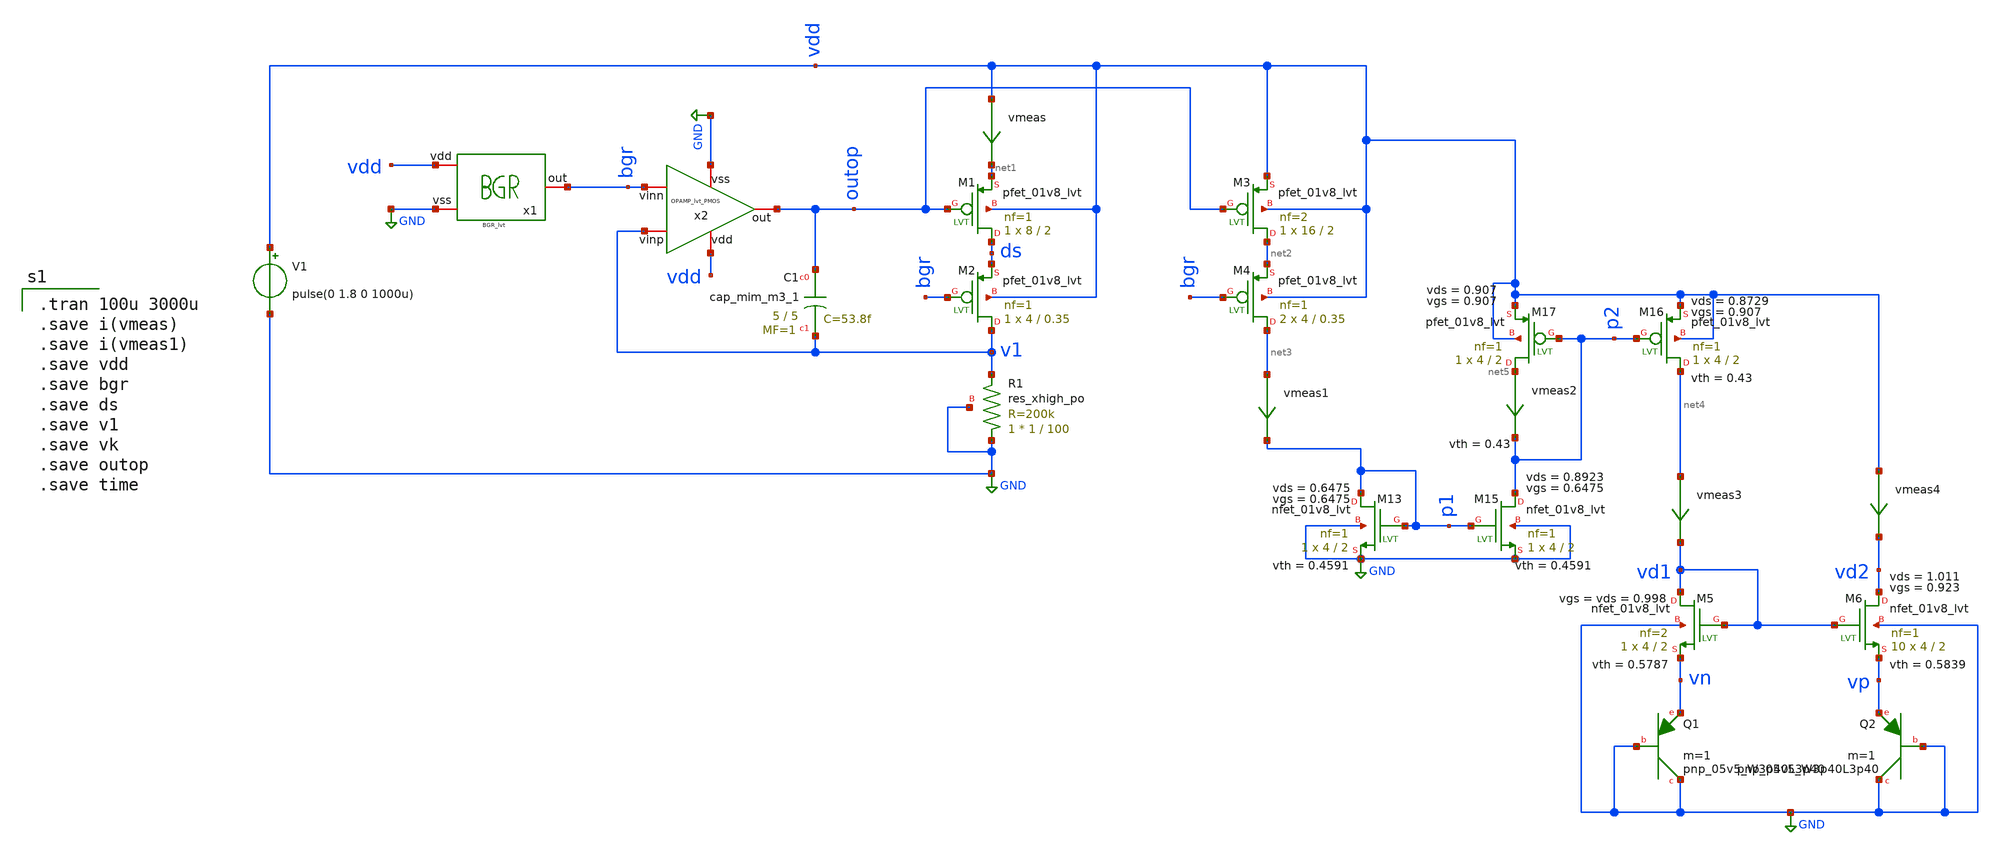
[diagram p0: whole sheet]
** sch_path: ANOTHER_SOLUTIONS_CONSIDERED/ANOTHER_BIAS_FOR_TEMPERATURE_SENSOR/CURRENT_SOURCE_FULL/XSCHEM/current_source_design_tb_ramp.sch
**.subckt current_source_design_tb_ramp
V1 vdd GND pulse(0 1.8 0 1000u)
vmeas vdd net1 0
.save i(vmeas)
XC1 outop v1 sky130_fd_pr__cap_mim_m3_1 W=5 L=5 MF=1 m=1
XM1 ds outop net1 vdd sky130_fd_pr__pfet_01v8_lvt L=2 W=8 nf=1 ad='int((nf+1)/2) * W/nf * 0.29' as='int((nf+2)/2) * W/nf * 0.29'
+ pd='2*int((nf+1)/2) * (W/nf + 0.29)' ps='2*int((nf+2)/2) * (W/nf + 0.29)' nrd='0.29 / W' nrs='0.29 / W'
+ sa=0 sb=0 sd=0 mult=1 m=1
XM2 v1 bgr ds vdd sky130_fd_pr__pfet_01v8_lvt L=0.35 W=4 nf=1 ad='int((nf+1)/2) * W/nf * 0.29' as='int((nf+2)/2) * W/nf * 0.29'
+ pd='2*int((nf+1)/2) * (W/nf + 0.29)' ps='2*int((nf+2)/2) * (W/nf + 0.29)' nrd='0.29 / W' nrs='0.29 / W'
+ sa=0 sb=0 sd=0 mult=1 m=1
XR1 GND v1 GND sky130_fd_pr__res_xhigh_po W=1 L=100 mult=1 m=1
XM3 net2 outop vdd vdd sky130_fd_pr__pfet_01v8_lvt L=2 W=16 nf=2 ad='int((nf+1)/2) * W/nf * 0.29' as='int((nf+2)/2) * W/nf * 0.29'
+ pd='2*int((nf+1)/2) * (W/nf + 0.29)' ps='2*int((nf+2)/2) * (W/nf + 0.29)' nrd='0.29 / W' nrs='0.29 / W'
+ sa=0 sb=0 sd=0 mult=1 m=1
XM4 net3 bgr net2 vdd sky130_fd_pr__pfet_01v8_lvt L=0.35 W=4 nf=1 ad='int((nf+1)/2) * W/nf * 0.29' as='int((nf+2)/2) * W/nf * 0.29'
+ pd='2*int((nf+1)/2) * (W/nf + 0.29)' ps='2*int((nf+2)/2) * (W/nf + 0.29)' nrd='0.29 / W' nrs='0.29 / W'
+ sa=0 sb=0 sd=0 mult=2 m=2
vmeas1 net3 p1 0
.save i(vmeas1)
x1 vdd bgr GND BGR_lvt
x2 vdd bgr v1 outop GND OPAMP_lvt_PMOS
XM5 vd1 vd1 vn GND sky130_fd_pr__nfet_01v8_lvt L=2 W=4 nf=2 ad='int((nf+1)/2) * W/nf * 0.29' as='int((nf+2)/2) * W/nf * 0.29'
+ pd='2*int((nf+1)/2) * (W/nf + 0.29)' ps='2*int((nf+2)/2) * (W/nf + 0.29)' nrd='0.29 / W' nrs='0.29 / W'
+ sa=0 sb=0 sd=0 mult=1 m=1
XQ1 GND GND vn sky130_fd_pr__pnp_05v5_W3p40L3p40 m=1
XM6 vd2 vd1 vp GND sky130_fd_pr__nfet_01v8_lvt L=2 W=4 nf=1 ad='int((nf+1)/2) * W/nf * 0.29' as='int((nf+2)/2) * W/nf * 0.29'
+ pd='2*int((nf+1)/2) * (W/nf + 0.29)' ps='2*int((nf+2)/2) * (W/nf + 0.29)' nrd='0.29 / W' nrs='0.29 / W'
+ sa=0 sb=0 sd=0 mult=10 m=10
XQ2 GND GND vp sky130_fd_pr__pnp_05v5_W3p40L3p40 m=1
vmeas4 vdd vd2 0
.save i(vmeas4)
vmeas3 net4 vd1 0
.save i(vmeas3)
XM13 p1 p1 GND GND sky130_fd_pr__nfet_01v8_lvt L=2 W=4 nf=1 ad='int((nf+1)/2) * W/nf * 0.29' as='int((nf+2)/2) * W/nf * 0.29'
+ pd='2*int((nf+1)/2) * (W/nf + 0.29)' ps='2*int((nf+2)/2) * (W/nf + 0.29)' nrd='0.29 / W' nrs='0.29 / W'
+ sa=0 sb=0 sd=0 mult=1 m=1
XM15 p2 p1 GND GND sky130_fd_pr__nfet_01v8_lvt L=2 W=4 nf=1 ad='int((nf+1)/2) * W/nf * 0.29' as='int((nf+2)/2) * W/nf * 0.29'
+ pd='2*int((nf+1)/2) * (W/nf + 0.29)' ps='2*int((nf+2)/2) * (W/nf + 0.29)' nrd='0.29 / W' nrs='0.29 / W'
+ sa=0 sb=0 sd=0 mult=1 m=1
XM17 net5 p2 vdd vdd sky130_fd_pr__pfet_01v8_lvt L=2 W=4 nf=1 ad='int((nf+1)/2) * W/nf * 0.29' as='int((nf+2)/2) * W/nf * 0.29'
+ pd='2*int((nf+1)/2) * (W/nf + 0.29)' ps='2*int((nf+2)/2) * (W/nf + 0.29)' nrd='0.29 / W' nrs='0.29 / W'
+ sa=0 sb=0 sd=0 mult=1 m=1
XM16 net4 p2 vdd vdd sky130_fd_pr__pfet_01v8_lvt L=2 W=4 nf=1 ad='int((nf+1)/2) * W/nf * 0.29' as='int((nf+2)/2) * W/nf * 0.29'
+ pd='2*int((nf+1)/2) * (W/nf + 0.29)' ps='2*int((nf+2)/2) * (W/nf + 0.29)' nrd='0.29 / W' nrs='0.29 / W'
+ sa=0 sb=0 sd=0 mult=1 m=1
vmeas2 net5 p2 0
.save i(vmeas2)
**** begin user architecture code

.tran 100u 3000u
.save i(vmeas)
.save i(vmeas1)
.save vdd
.save bgr
.save ds
.save v1
.save vk
.save outop
.save time


** opencircuitdesign pdks install
.lib $::SKYWATER_MODELS/sky130.lib.spice tt


**** end user architecture code
**.ends
.GLOBAL GND
.end
